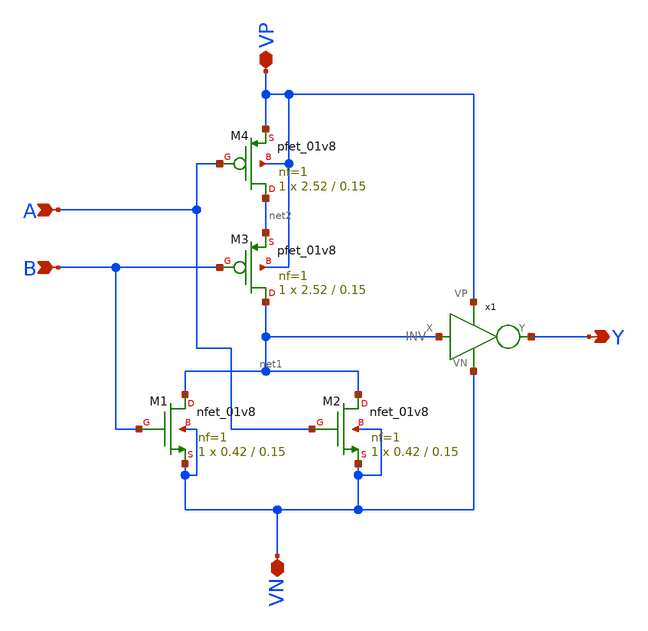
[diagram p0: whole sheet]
** sch_path: component/OR2/OR_2.sch
**.subckt OR_2 VP VN A B Y
*.iopin VP
*.iopin VN
*.ipin A
*.ipin B
*.opin Y
XM1 net1 B VN VN sky130_fd_pr__nfet_01v8 L=0.15 W=0.42 nf=1 ad='int((nf+1)/2) * W/nf * 0.29' as='int((nf+2)/2) * W/nf * 0.29'
+ pd='2*int((nf+1)/2) * (W/nf + 0.29)' ps='2*int((nf+2)/2) * (W/nf + 0.29)' nrd='0.29 / W' nrs='0.29 / W'
+ sa=0 sb=0 sd=0 mult=1 m=1
XM2 net1 A VN VN sky130_fd_pr__nfet_01v8 L=0.15 W=0.42 nf=1 ad='int((nf+1)/2) * W/nf * 0.29' as='int((nf+2)/2) * W/nf * 0.29'
+ pd='2*int((nf+1)/2) * (W/nf + 0.29)' ps='2*int((nf+2)/2) * (W/nf + 0.29)' nrd='0.29 / W' nrs='0.29 / W'
+ sa=0 sb=0 sd=0 mult=1 m=1
XM3 net1 B net2 VP sky130_fd_pr__pfet_01v8 L=0.15 W=2.52 nf=1 ad='int((nf+1)/2) * W/nf * 0.29' as='int((nf+2)/2) * W/nf * 0.29'
+ pd='2*int((nf+1)/2) * (W/nf + 0.29)' ps='2*int((nf+2)/2) * (W/nf + 0.29)' nrd='0.29 / W' nrs='0.29 / W'
+ sa=0 sb=0 sd=0 mult=1 m=1
XM4 net2 A VP VP sky130_fd_pr__pfet_01v8 L=0.15 W=2.52 nf=1 ad='int((nf+1)/2) * W/nf * 0.29' as='int((nf+2)/2) * W/nf * 0.29'
+ pd='2*int((nf+1)/2) * (W/nf + 0.29)' ps='2*int((nf+2)/2) * (W/nf + 0.29)' nrd='0.29 / W' nrs='0.29 / W'
+ sa=0 sb=0 sd=0 mult=1 m=1
x1 net1 Y VP VN INV
**.ends

* expanding   symbol:  component/Inverter/INV.sym # of pins=4
** sym_path: component/Inverter/INV.sym
** sch_path: component/Inverter/INV.sch
.subckt INV X Y VP VN
*.ipin X
*.opin Y
*.iopin VN
*.iopin VP
XM8 Y X VP VP sky130_fd_pr__pfet_01v8 L=.18 W=1.512 nf=1 ad='int((nf+1)/2) * W/nf * 0.29' as='int((nf+2)/2) * W/nf * 0.29'
+ pd='2*int((nf+1)/2) * (W/nf + 0.29)' ps='2*int((nf+2)/2) * (W/nf + 0.29)' nrd='0.29 / W' nrs='0.29 / W'
+ sa=0 sb=0 sd=0 mult=1 m=1
XM4 Y X VN VN sky130_fd_pr__nfet_01v8 L=0.18 W=0.42 nf=1 ad='int((nf+1)/2) * W/nf * 0.29' as='int((nf+2)/2) * W/nf * 0.29'
+ pd='2*int((nf+1)/2) * (W/nf + 0.29)' ps='2*int((nf+2)/2) * (W/nf + 0.29)' nrd='0.29 / W' nrs='0.29 / W'
+ sa=0 sb=0 sd=0 mult=1 m=1
.ends

.end
